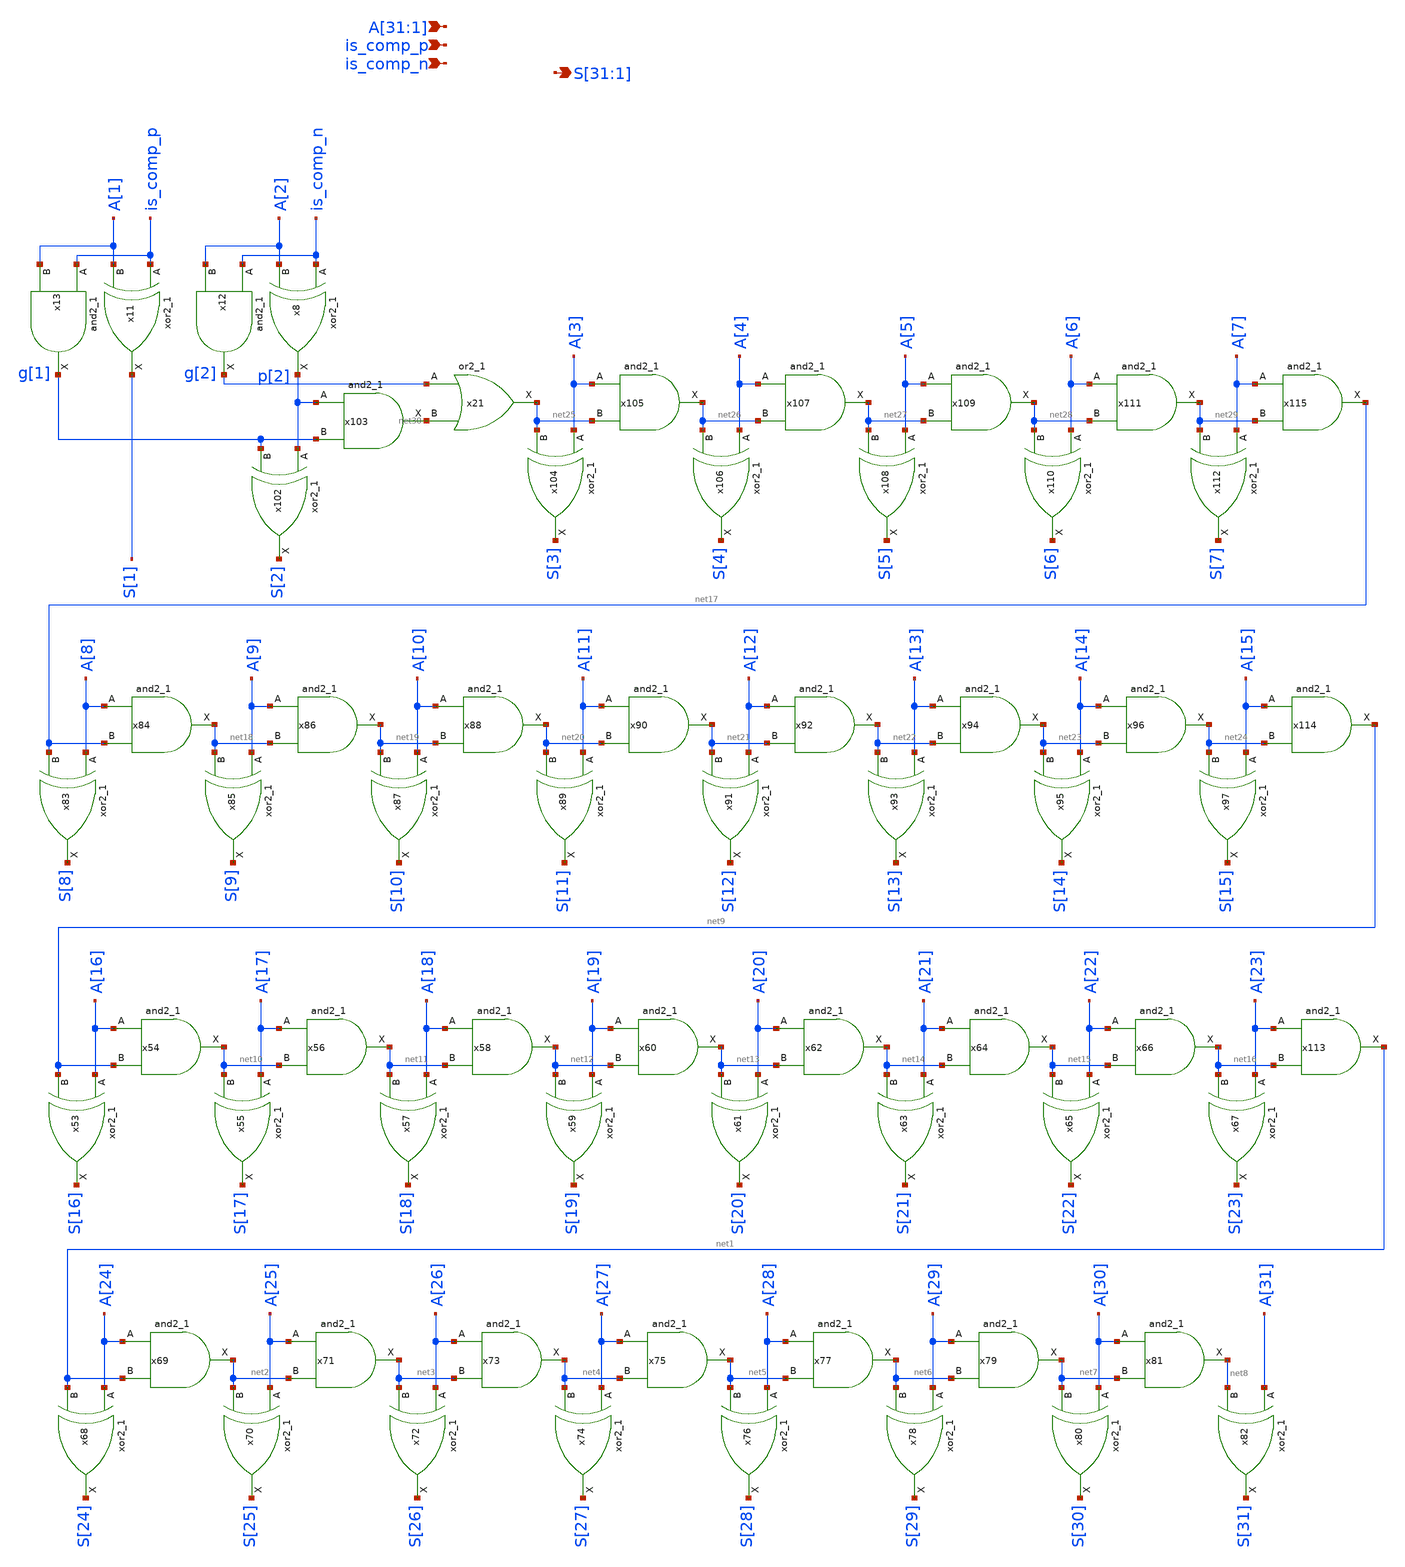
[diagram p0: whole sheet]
** sch_path: blocks/pc_inc/pc_inc.sch
**.subckt pc_inc
*+ S[31],S[30],S[29],S[28],S[27],S[26],S[25],S[24],S[23],S[22],S[21],S[20],S[19],S[18],S[17],S[16],S[15],S[14],S[13],S[12],S[11],S[10],S[9],S[8],S[7],S[6],S[5],S[4],S[3],S[2],S[1]
*+ A[31],A[30],A[29],A[28],A[27],A[26],A[25],A[24],A[23],A[22],A[21],A[20],A[19],A[18],A[17],A[16],A[15],A[14],A[13],A[12],A[11],A[10],A[9],A[8],A[7],A[6],A[5],A[4],A[3],A[2],A[1] is_comp_p is_comp_n
*.opin
*+ S[31],S[30],S[29],S[28],S[27],S[26],S[25],S[24],S[23],S[22],S[21],S[20],S[19],S[18],S[17],S[16],S[15],S[14],S[13],S[12],S[11],S[10],S[9],S[8],S[7],S[6],S[5],S[4],S[3],S[2],S[1]
*.ipin
*+ A[31],A[30],A[29],A[28],A[27],A[26],A[25],A[24],A[23],A[22],A[21],A[20],A[19],A[18],A[17],A[16],A[15],A[14],A[13],A[12],A[11],A[10],A[9],A[8],A[7],A[6],A[5],A[4],A[3],A[2],A[1]
*.ipin is_comp_p
*.ipin is_comp_n
x21 g[2] net30 VSS VSS VCC VCC net25 sky130_fd_sc_hd__or2_1
x68 A[24] net1 VSS VSS VCC VCC S[24] sky130_fd_sc_hd__xor2_1
x69 A[24] net1 VSS VSS VCC VCC net2 sky130_fd_sc_hd__and2_1
x70 A[25] net2 VSS VSS VCC VCC S[25] sky130_fd_sc_hd__xor2_1
x71 A[25] net2 VSS VSS VCC VCC net3 sky130_fd_sc_hd__and2_1
x72 A[26] net3 VSS VSS VCC VCC S[26] sky130_fd_sc_hd__xor2_1
x73 A[26] net3 VSS VSS VCC VCC net4 sky130_fd_sc_hd__and2_1
x74 A[27] net4 VSS VSS VCC VCC S[27] sky130_fd_sc_hd__xor2_1
x75 A[27] net4 VSS VSS VCC VCC net5 sky130_fd_sc_hd__and2_1
x76 A[28] net5 VSS VSS VCC VCC S[28] sky130_fd_sc_hd__xor2_1
x77 A[28] net5 VSS VSS VCC VCC net6 sky130_fd_sc_hd__and2_1
x78 A[29] net6 VSS VSS VCC VCC S[29] sky130_fd_sc_hd__xor2_1
x79 A[29] net6 VSS VSS VCC VCC net7 sky130_fd_sc_hd__and2_1
x80 A[30] net7 VSS VSS VCC VCC S[30] sky130_fd_sc_hd__xor2_1
x81 A[30] net7 VSS VSS VCC VCC net8 sky130_fd_sc_hd__and2_1
x82 A[31] net8 VSS VSS VCC VCC S[31] sky130_fd_sc_hd__xor2_1
x53 A[16] net9 VSS VSS VCC VCC S[16] sky130_fd_sc_hd__xor2_1
x54 A[16] net9 VSS VSS VCC VCC net10 sky130_fd_sc_hd__and2_1
x55 A[17] net10 VSS VSS VCC VCC S[17] sky130_fd_sc_hd__xor2_1
x56 A[17] net10 VSS VSS VCC VCC net11 sky130_fd_sc_hd__and2_1
x57 A[18] net11 VSS VSS VCC VCC S[18] sky130_fd_sc_hd__xor2_1
x58 A[18] net11 VSS VSS VCC VCC net12 sky130_fd_sc_hd__and2_1
x59 A[19] net12 VSS VSS VCC VCC S[19] sky130_fd_sc_hd__xor2_1
x60 A[19] net12 VSS VSS VCC VCC net13 sky130_fd_sc_hd__and2_1
x61 A[20] net13 VSS VSS VCC VCC S[20] sky130_fd_sc_hd__xor2_1
x62 A[20] net13 VSS VSS VCC VCC net14 sky130_fd_sc_hd__and2_1
x63 A[21] net14 VSS VSS VCC VCC S[21] sky130_fd_sc_hd__xor2_1
x64 A[21] net14 VSS VSS VCC VCC net15 sky130_fd_sc_hd__and2_1
x65 A[22] net15 VSS VSS VCC VCC S[22] sky130_fd_sc_hd__xor2_1
x66 A[22] net15 VSS VSS VCC VCC net16 sky130_fd_sc_hd__and2_1
x67 A[23] net16 VSS VSS VCC VCC S[23] sky130_fd_sc_hd__xor2_1
x83 A[8] net17 VSS VSS VCC VCC S[8] sky130_fd_sc_hd__xor2_1
x84 A[8] net17 VSS VSS VCC VCC net18 sky130_fd_sc_hd__and2_1
x85 A[9] net18 VSS VSS VCC VCC S[9] sky130_fd_sc_hd__xor2_1
x86 A[9] net18 VSS VSS VCC VCC net19 sky130_fd_sc_hd__and2_1
x87 A[10] net19 VSS VSS VCC VCC S[10] sky130_fd_sc_hd__xor2_1
x88 A[10] net19 VSS VSS VCC VCC net20 sky130_fd_sc_hd__and2_1
x89 A[11] net20 VSS VSS VCC VCC S[11] sky130_fd_sc_hd__xor2_1
x90 A[11] net20 VSS VSS VCC VCC net21 sky130_fd_sc_hd__and2_1
x91 A[12] net21 VSS VSS VCC VCC S[12] sky130_fd_sc_hd__xor2_1
x92 A[12] net21 VSS VSS VCC VCC net22 sky130_fd_sc_hd__and2_1
x93 A[13] net22 VSS VSS VCC VCC S[13] sky130_fd_sc_hd__xor2_1
x94 A[13] net22 VSS VSS VCC VCC net23 sky130_fd_sc_hd__and2_1
x95 A[14] net23 VSS VSS VCC VCC S[14] sky130_fd_sc_hd__xor2_1
x96 A[14] net23 VSS VSS VCC VCC net24 sky130_fd_sc_hd__and2_1
x97 A[15] net24 VSS VSS VCC VCC S[15] sky130_fd_sc_hd__xor2_1
x102 p[2] g[1] VSS VSS VCC VCC S[2] sky130_fd_sc_hd__xor2_1
x103 p[2] g[1] VSS VSS VCC VCC net30 sky130_fd_sc_hd__and2_1
x104 A[3] net25 VSS VSS VCC VCC S[3] sky130_fd_sc_hd__xor2_1
x105 A[3] net25 VSS VSS VCC VCC net26 sky130_fd_sc_hd__and2_1
x106 A[4] net26 VSS VSS VCC VCC S[4] sky130_fd_sc_hd__xor2_1
x107 A[4] net26 VSS VSS VCC VCC net27 sky130_fd_sc_hd__and2_1
x108 A[5] net27 VSS VSS VCC VCC S[5] sky130_fd_sc_hd__xor2_1
x109 A[5] net27 VSS VSS VCC VCC net28 sky130_fd_sc_hd__and2_1
x110 A[6] net28 VSS VSS VCC VCC S[6] sky130_fd_sc_hd__xor2_1
x111 A[6] net28 VSS VSS VCC VCC net29 sky130_fd_sc_hd__and2_1
x112 A[7] net29 VSS VSS VCC VCC S[7] sky130_fd_sc_hd__xor2_1
x113 A[23] net16 VSS VSS VCC VCC net1 sky130_fd_sc_hd__and2_1
x114 A[15] net24 VSS VSS VCC VCC net9 sky130_fd_sc_hd__and2_1
x115 A[7] net29 VSS VSS VCC VCC net17 sky130_fd_sc_hd__and2_1
x8 is_comp_n A[2] VSS VSS VCC VCC p[2] sky130_fd_sc_hd__xor2_1
x11 is_comp_p A[1] VSS VSS VCC VCC S[1] sky130_fd_sc_hd__xor2_1
x12 is_comp_n A[2] VSS VSS VCC VCC g[2] sky130_fd_sc_hd__and2_1
x13 is_comp_p A[1] VSS VSS VCC VCC g[1] sky130_fd_sc_hd__and2_1
**.ends
.end
